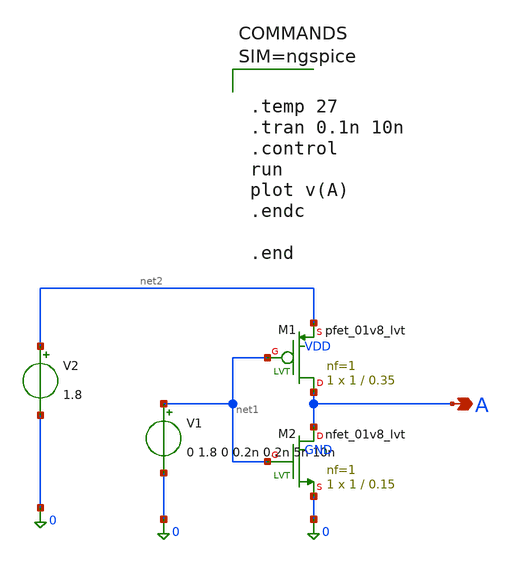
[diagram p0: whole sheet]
** sch_path: sar-adc/vni.sch
**.subckt vni A
*.opin A
V1 net1 0 0 1.8 0 0.2n 0.2n 5n 10n
V2 net2 0 1.8
XM1 A net1 net2 VDD sky130_fd_pr__pfet_01v8_lvt L=0.35 W=1 nf=1 ad='int((1 + 1)/2) * 1 / 1 * 0.29' as='int((1 + 2)/2) * 1 / 1 * 0.29'
+ pd='2*int((1 + 1)/2) * (1 / 1 + 0.29)' ps='2*int((1 + 2)/2) * (1 / 1 + 0.29)' nrd='0.29 / 1 ' nrs='0.29 / 1 '
+ sa=0 sb=0 sd=0 mult=1 m=1
XM2 A net1 0 GND sky130_fd_pr__nfet_01v8_lvt L=0.15 W=1 nf=1 ad='int((1 + 1)/2) * 1 / 1 * 0.29' as='int((1 + 2)/2) * 1 / 1 * 0.29'
+ pd='2*int((1 + 1)/2) * (1 / 1 + 0.29)' ps='2*int((1 + 2)/2) * (1 / 1 + 0.29)' nrd='0.29 / 1 ' nrs='0.29 / 1 '
+ sa=0 sb=0 sd=0 mult=1 m=1
**** begin user architecture code



.temp 27
.tran 0.1n 10n
.control
run
plot v(A)
.endc

.end





**** end user architecture code
**.ends
.end
